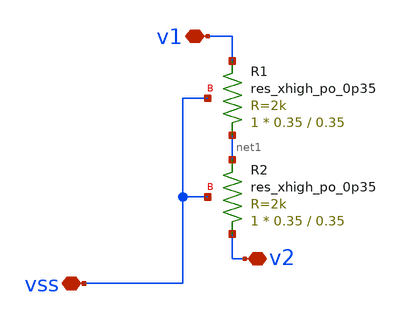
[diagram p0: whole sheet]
** sch_path: xschem_final/div_voltage.sch
**.subckt div_voltage vss v1 v2
*.iopin vss
*.iopin v1
*.iopin v2
XR1 net1 v1 vss sky130_fd_pr__res_xhigh_po_0p35 L=0.35 mult=1 m=1
XR2 v2 net1 vss sky130_fd_pr__res_xhigh_po_0p35 L=0.35 mult=1 m=1
**.ends
.end
